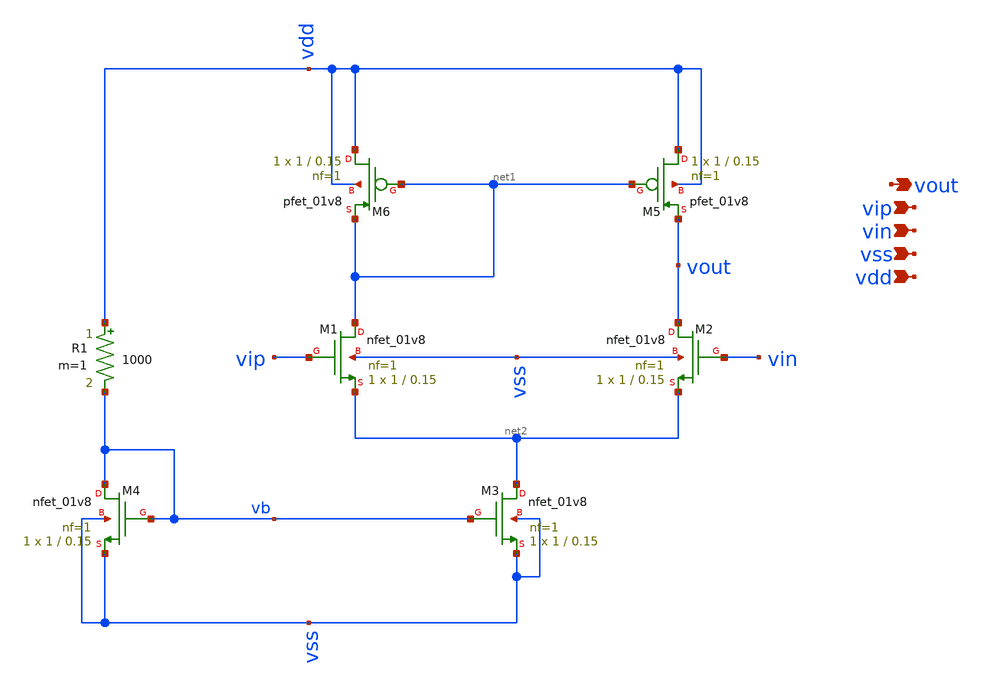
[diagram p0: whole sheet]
** sch_path: pre_layout_sim/ota.sch
**.subckt ota vin vout vip vdd vss
*.ipin vin
*.opin vout
*.ipin vip
*.ipin vdd
*.ipin vss
XM1 net1 vip net2 vss sky130_fd_pr__nfet_01v8 L=0.15 W=1 nf=1 ad='int((1 + 1)/2) * 1 / 1 * 0.29' as='int((1 + 2)/2) * 1 / 1 * 0.29'
+ pd='2*int((1 + 1)/2) * (1 / 1 + 0.29)' ps='2*int((1 + 2)/2) * (1 / 1 + 0.29)' nrd='0.29 / 1 ' nrs='0.29 / 1 '
+ sa=0 sb=0 sd=0 mult=1 m=1
XM2 vout vin net2 vss sky130_fd_pr__nfet_01v8 L=0.15 W=1 nf=1 ad='int((1 + 1)/2) * 1 / 1 * 0.29' as='int((1 + 2)/2) * 1 / 1 * 0.29'
+ pd='2*int((1 + 1)/2) * (1 / 1 + 0.29)' ps='2*int((1 + 2)/2) * (1 / 1 + 0.29)' nrd='0.29 / 1 ' nrs='0.29 / 1 '
+ sa=0 sb=0 sd=0 mult=1 m=1
XM3 net2 vb vss vss sky130_fd_pr__nfet_01v8 L=0.15 W=1 nf=1 ad='int((1 + 1)/2) * 1 / 1 * 0.29' as='int((1 + 2)/2) * 1 / 1 * 0.29'
+ pd='2*int((1 + 1)/2) * (1 / 1 + 0.29)' ps='2*int((1 + 2)/2) * (1 / 1 + 0.29)' nrd='0.29 / 1 ' nrs='0.29 / 1 '
+ sa=0 sb=0 sd=0 mult=1 m=1
XM5 vdd net1 vout vdd sky130_fd_pr__pfet_01v8 L=0.15 W=1 nf=1 ad='int((1 + 1)/2) * 1 / 1 * 0.29' as='int((1 + 2)/2) * 1 / 1 * 0.29'
+ pd='2*int((1 + 1)/2) * (1 / 1 + 0.29)' ps='2*int((1 + 2)/2) * (1 / 1 + 0.29)' nrd='0.29 / 1 ' nrs='0.29 / 1 '
+ sa=0 sb=0 sd=0 mult=1 m=1
XM6 vdd net1 net1 vdd sky130_fd_pr__pfet_01v8 L=0.15 W=1 nf=1 ad='int((1 + 1)/2) * 1 / 1 * 0.29' as='int((1 + 2)/2) * 1 / 1 * 0.29'
+ pd='2*int((1 + 1)/2) * (1 / 1 + 0.29)' ps='2*int((1 + 2)/2) * (1 / 1 + 0.29)' nrd='0.29 / 1 ' nrs='0.29 / 1 '
+ sa=0 sb=0 sd=0 mult=1 m=1
XM4 vb vb vss vss sky130_fd_pr__nfet_01v8 L=0.15 W=1 nf=1 ad='int((1 + 1)/2) * 1 / 1 * 0.29' as='int((1 + 2)/2) * 1 / 1 * 0.29'
+ pd='2*int((1 + 1)/2) * (1 / 1 + 0.29)' ps='2*int((1 + 2)/2) * (1 / 1 + 0.29)' nrd='0.29 / 1 ' nrs='0.29 / 1 '
+ sa=0 sb=0 sd=0 mult=1 m=1
R1 vdd vb 1000 m=1
**.ends
.end
